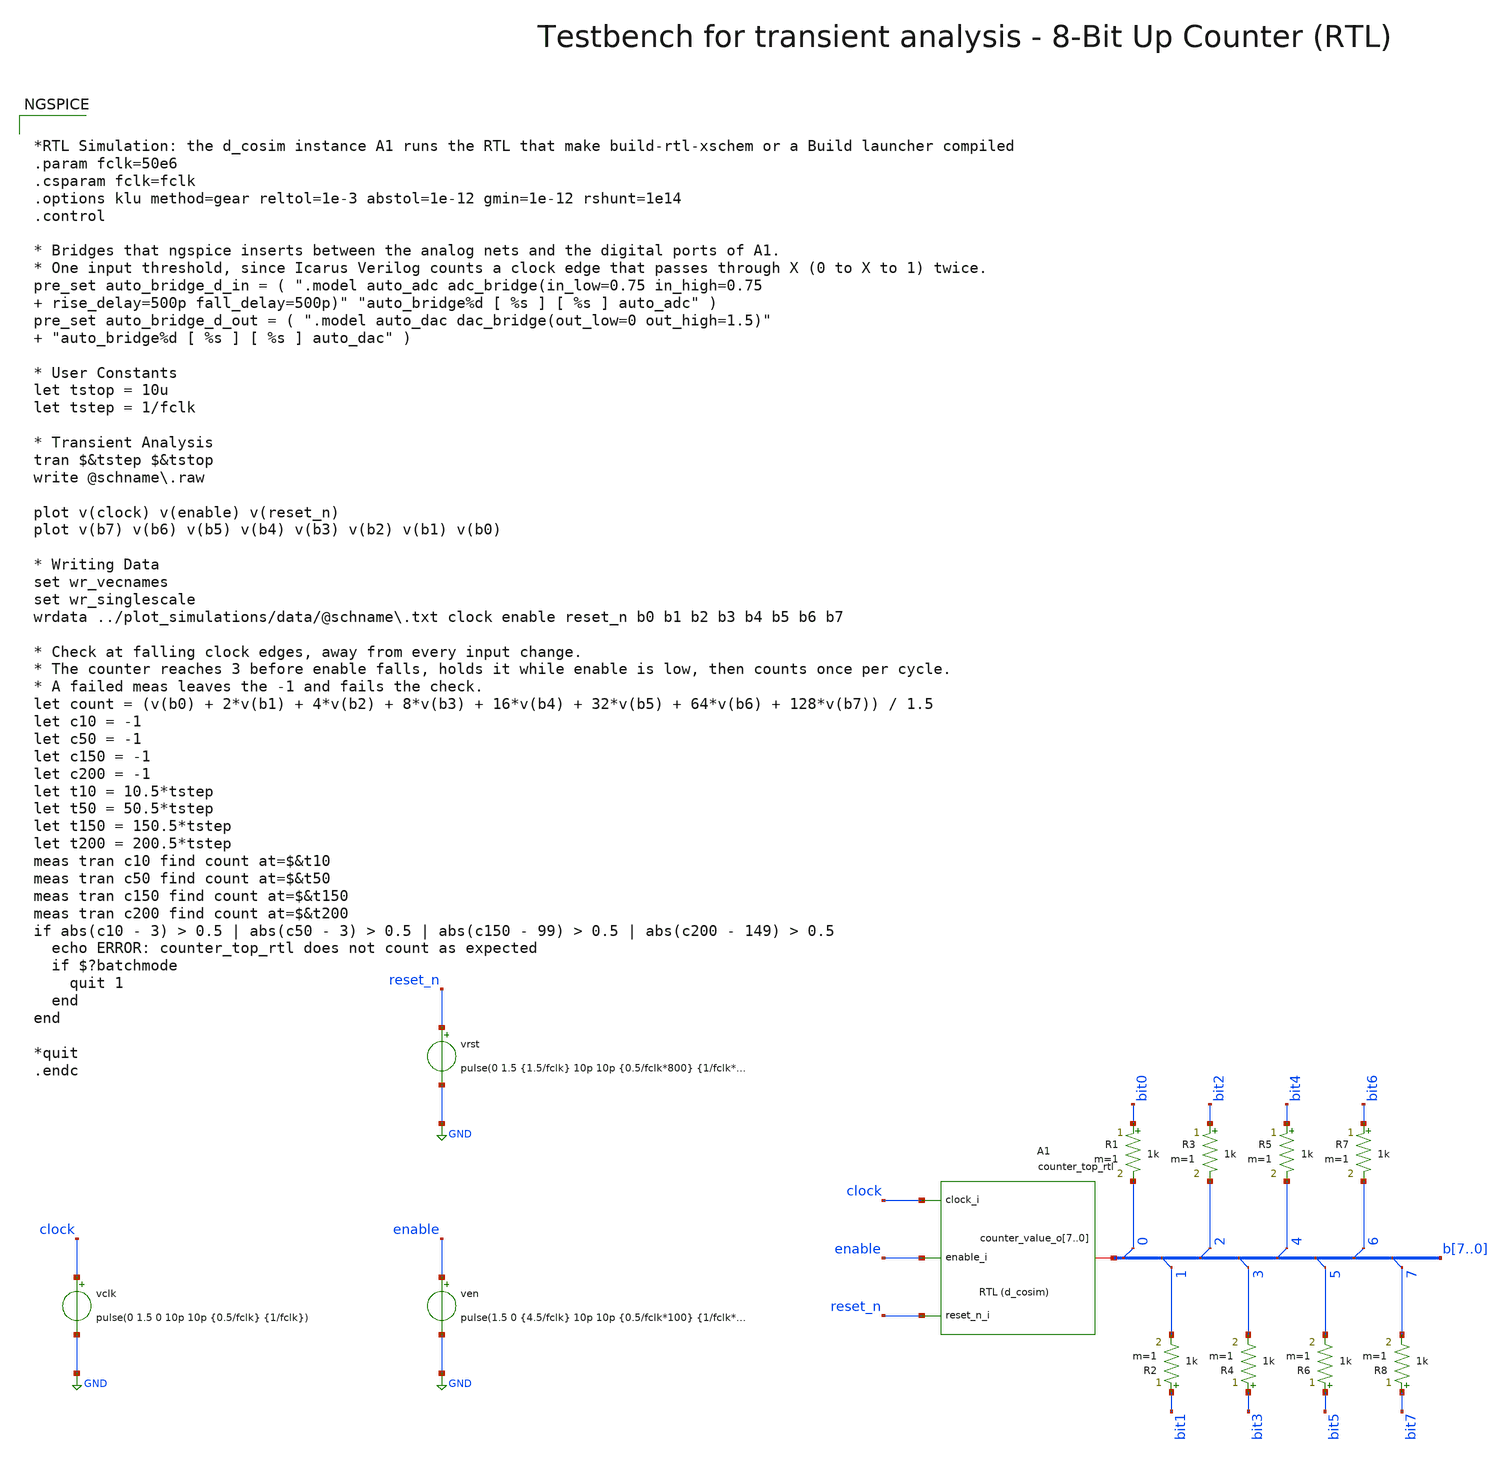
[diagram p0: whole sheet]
** sch_path: macros/counter/testbenches/xschem/counter_top_tb_tran_rtl.sch
**.subckt counter_top_tb_tran_rtl
vclk clock GND pulse(0 1.5 0 10p 10p {0.5/fclk} {1/fclk})
vrst reset_n GND pulse(0 1.5 {1.5/fclk} 10p 10p {0.5/fclk*800} {1/fclk*600} 1)
ven enable GND pulse(1.5 0 {4.5/fclk} 10p 10p {0.5/fclk*100} {1/fclk*100} 1)
A1 [ clock reset_n enable ] [ b7 b6 b5 b4 b3 b2 b1 b0 ] counter_top_rtl
* tap: b[7..0] --> b0
R1 bit0 b0 1k m=1
* tap: b[7..0] --> b1
R2 bit1 b1 1k m=1
* tap: b[7..0] --> b2
R3 bit2 b2 1k m=1
* tap: b[7..0] --> b3
R4 bit3 b3 1k m=1
* tap: b[7..0] --> b4
R5 bit4 b4 1k m=1
* tap: b[7..0] --> b5
R6 bit5 b5 1k m=1
* tap: b[7..0] --> b6
R7 bit6 b6 1k m=1
* tap: b[7..0] --> b7
R8 bit7 b7 1k m=1
**** begin user architecture code


*RTL Simulation: the d_cosim instance A1 runs the RTL that make build-rtl-xschem or a Build launcher
*+ compiled
.param fclk=50e6
.csparam fclk=fclk
.options klu method=gear reltol=1e-3 abstol=1e-12 gmin=1e-12 rshunt=1e14
.control

* Bridges that ngspice inserts between the analog nets and the digital ports of A1.
* One input threshold, since Icarus Verilog counts a clock edge that passes through X (0 to X to 1)
*+ twice.
pre_set auto_bridge_d_in = ( ".model auto_adc adc_bridge(in_low=0.75 in_high=0.75  rise_delay=500p
+ fall_delay=500p)" "auto_bridge%d [ %s ] [ %s ] auto_adc" )
pre_set auto_bridge_d_out = ( ".model auto_dac dac_bridge(out_low=0 out_high=1.5)"  "auto_bridge%d [
+ %s ] [ %s ] auto_dac" )

* User Constants
let tstop = 10u
let tstep = 1/fclk

* Transient Analysis
tran $&tstep $&tstop
write @schname\.raw

plot v(clock) v(enable) v(reset_n)
plot v(b7) v(b6) v(b5) v(b4) v(b3) v(b2) v(b1) v(b0)

* Writing Data
set wr_vecnames
set wr_singlescale
wrdata ../plot_simulations/data/@schname\.txt clock enable reset_n b0 b1 b2 b3 b4 b5 b6 b7

* Check at falling clock edges, away from every input change.
* The counter reaches 3 before enable falls, holds it while enable is low, then counts once per
*+ cycle.
* A failed meas leaves the -1 and fails the check.
let count = (v(b0) + 2*v(b1) + 4*v(b2) + 8*v(b3) + 16*v(b4) + 32*v(b5) + 64*v(b6) + 128*v(b7)) / 1.5
let c10 = -1
let c50 = -1
let c150 = -1
let c200 = -1
let t10 = 10.5*tstep
let t50 = 50.5*tstep
let t150 = 150.5*tstep
let t200 = 200.5*tstep
meas tran c10 find count at=$&t10
meas tran c50 find count at=$&t50
meas tran c150 find count at=$&t150
meas tran c200 find count at=$&t200
if abs(c10 - 3) > 0.5 | abs(c50 - 3) > 0.5 | abs(c150 - 99) > 0.5 | abs(c200 - 149) > 0.5
  echo ERROR: counter_top_rtl does not count as expected
  if $?batchmode
    quit 1
  end
end

*quit
.endc

**** end user architecture code
**.ends
.GLOBAL GND
**** begin user architecture code
.model counter_top_rtl d_cosim  simulation="ivlng" sim_args=["counter_top.vvp"]
**** end user architecture code
.end
